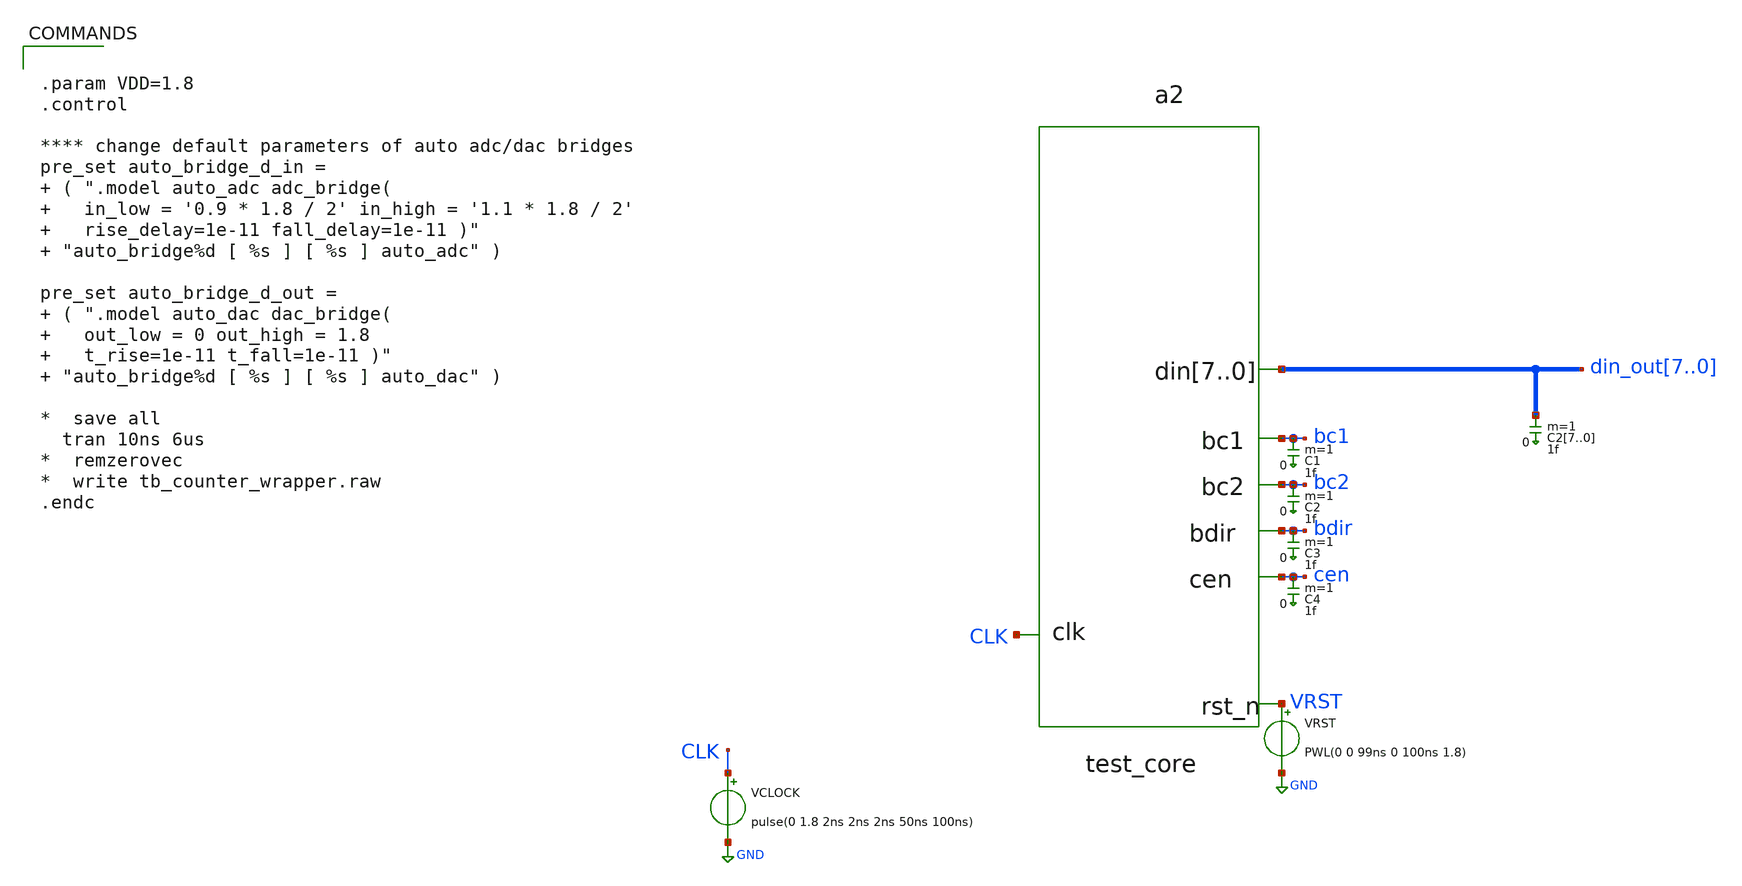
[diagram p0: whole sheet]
** sch_path: xschem/testbench_test_core.sch
**.subckt testbench_test_core
VRST VRST GND PWL(0 0 99ns 0 100ns 1.8)
a2 [ CLK VRST ] [ cen bdir bc1 bc2 din_out7 din_out6 din_out5 din_out4 din_out3 din_out2 din_out1
+ din_out0 ] test_core
VCLOCK CLK GND pulse(0 1.8 2ns 2ns 2ns 50ns 100ns)
C27 din_out7 0 1f m=1
C26 din_out6 0 1f m=1
C25 din_out5 0 1f m=1
C24 din_out4 0 1f m=1
C23 din_out3 0 1f m=1
C22 din_out2 0 1f m=1
C21 din_out1 0 1f m=1
C20 din_out0 0 1f m=1
C1 bc1 0 1f m=1
C2 bc2 0 1f m=1
C3 bdir 0 1f m=1
C4 cen 0 1f m=1
**** begin user architecture code


.param VDD=1.8
.control

**** change default parameters of auto adc/dac bridges
pre_set auto_bridge_d_in =  ( ".model auto_adc adc_bridge(    in_low = '0.9 * 1.8 / 2' in_high = '1.1 * 1.8 / 2'
+    rise_delay=1e-11 fall_delay=1e-11 )"  "auto_bridge%d [ %s ] [ %s ] auto_adc" )

pre_set auto_bridge_d_out =  ( ".model auto_dac dac_bridge(    out_low = 0 out_high = 1.8
+    t_rise=1e-11 t_fall=1e-11 )"  "auto_bridge%d [ %s ] [ %s ] auto_dac" )

*  save all
  tran 10ns 6us
*  remzerovec
*  write tb_counter_wrapper.raw
.endc


**** end user architecture code
**.ends
.GLOBAL GND
**** begin user architecture code
.model test_core d_cosim simulation="ivlng" sim_args=["test_core"]
**** end user architecture code
.end
